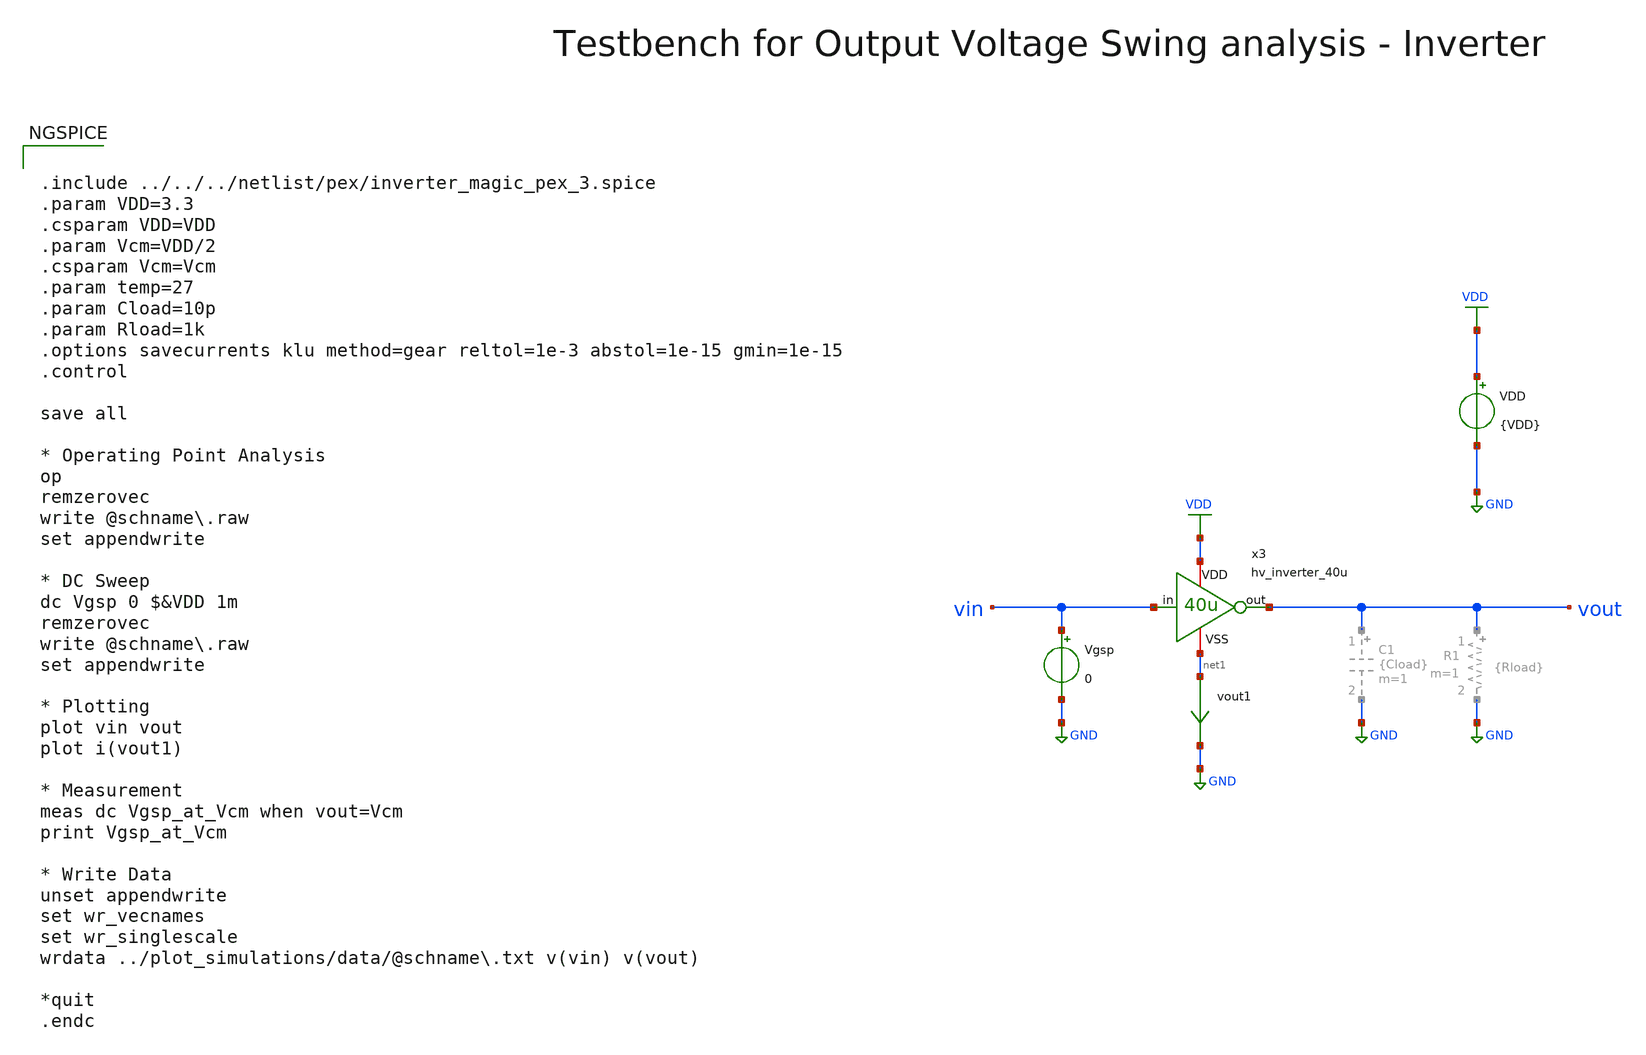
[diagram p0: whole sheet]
** sch_path: macros/heichips26_vcr/macros/switched_capacitor/testbenches/xschem/tb_hv_inverter_40u_dc.sch
**.subckt tb_hv_inverter_40u_dc
VDD VDD GND {VDD}
Vgsp vin GND 0
x3 VDD vin vout net1 hv_inverter_40u
vout1 net1 GND 0
.save i(vout1)
**** begin user architecture code


.include ../../../netlist/pex/inverter_magic_pex_3.spice
.param VDD=3.3
.csparam VDD=VDD
.param Vcm=VDD/2
.csparam Vcm=Vcm
.param temp=27
.param Cload=10p
.param Rload=1k
.options savecurrents klu method=gear reltol=1e-3 abstol=1e-15 gmin=1e-15
.control

save all

* Operating Point Analysis
op
remzerovec
write @schname\.raw
set appendwrite

* DC Sweep
dc Vgsp 0 $&VDD 1m
remzerovec
write @schname\.raw
set appendwrite

* Plotting
plot vin vout
plot i(vout1)

* Measurement
meas dc Vgsp_at_Vcm when vout=Vcm
print Vgsp_at_Vcm

* Write Data
unset appendwrite
set wr_vecnames
set wr_singlescale
wrdata ../plot_simulations/data/@schname\.txt v(vin) v(vout)

*quit
.endc



.lib cornerMOSlv.lib mos_tt
.lib cornerMOShv.lib mos_tt
.lib cornerRES.lib res_typ
.lib cornerDIO.lib dio_tt

**** end user architecture code
**.ends

* expanding   symbol:  hv_inverter_40u.sym # of pins=4
** sym_path: macros/heichips26_vcr/macros/switched_capacitor/schematic/xschem/hv_inverter_40u.sym
** sch_path: macros/heichips26_vcr/macros/switched_capacitor/schematic/xschem/hv_inverter_40u.sch
.subckt hv_inverter_40u VDD in out VSS
*.ipin in
*.iopin VDD
*.iopin VSS
*.opin out
XM2 out in VSS VSS sg13_hv_nmos w={n_w} l={n_l} ng={ng} m=1 mm_ok=1
XM3 out in VDD VDD sg13_hv_pmos w={p_w} l={p_l} ng={ng} m=1 mm_ok=1
**** begin user architecture code


.param w   = 10u
.param ng  = 4
.param n_ng = ng
.param n_w = {3u*n_ng}
.param n_l = 0.45u
.param p_ng = ng
.param p_w = {10u*p_ng}
.param p_l = 0.4u


**** end user architecture code
.ends

.GLOBAL GND
.GLOBAL VDD
.end
